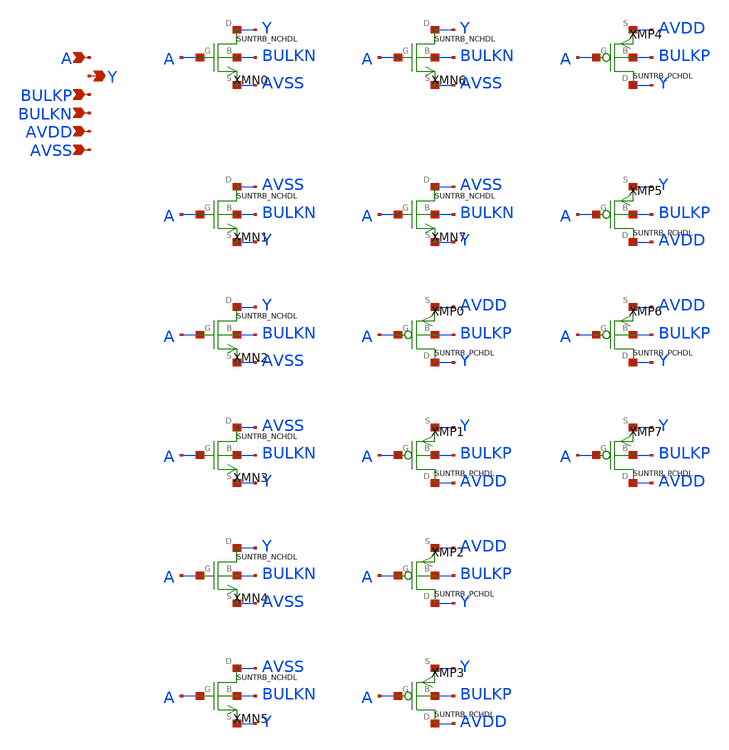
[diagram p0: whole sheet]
** sch_path: ip/sun_trb_sky130nm/design/SUN_TRB_SKY130NM/SUNTRB_IVX8_CV.sch
**.subckt SUNTRB_IVX8_CV A Y BULKP BULKN AVDD AVSS
*.ipin A
*.opin Y
*.ipin BULKP
*.ipin BULKN
*.ipin AVDD
*.ipin AVSS
XMN0 Y A AVSS BULKN SUNTRB_NCHDL xoffset=0 yoffset=0 angle=0
XMN1 AVSS A Y BULKN SUNTRB_NCHDL xoffset=0 yoffset=0 angle=0
XMN2 Y A AVSS BULKN SUNTRB_NCHDL xoffset=0 yoffset=0 angle=0
XMN3 AVSS A Y BULKN SUNTRB_NCHDL xoffset=0 yoffset=0 angle=0
XMN4 Y A AVSS BULKN SUNTRB_NCHDL xoffset=0 yoffset=0 angle=0
XMN5 AVSS A Y BULKN SUNTRB_NCHDL xoffset=0 yoffset=0 angle=0
XMN6 Y A AVSS BULKN SUNTRB_NCHDL xoffset=0 yoffset=0 angle=0
XMN7 AVSS A Y BULKN SUNTRB_NCHDL xoffset=0 yoffset=0 angle=0
XMP0 Y A AVDD BULKP SUNTRB_PCHDL xoffset=0 yoffset=0 angle=0
XMP1 AVDD A Y BULKP SUNTRB_PCHDL xoffset=0 yoffset=0 angle=0
XMP2 Y A AVDD BULKP SUNTRB_PCHDL xoffset=0 yoffset=0 angle=0
XMP3 AVDD A Y BULKP SUNTRB_PCHDL xoffset=0 yoffset=0 angle=0
XMP4 Y A AVDD BULKP SUNTRB_PCHDL xoffset=0 yoffset=0 angle=0
XMP5 AVDD A Y BULKP SUNTRB_PCHDL xoffset=0 yoffset=0 angle=0
XMP6 Y A AVDD BULKP SUNTRB_PCHDL xoffset=0 yoffset=0 angle=0
XMP7 AVDD A Y BULKP SUNTRB_PCHDL xoffset=0 yoffset=0 angle=0
**.ends
.end
